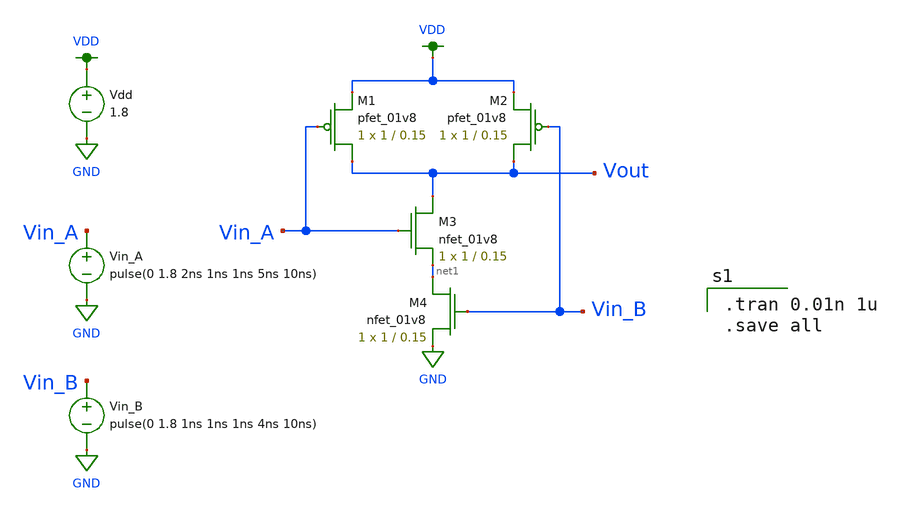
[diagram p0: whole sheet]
** sch_path: MP1/xschem/NAND_tran.sch
**.subckt NAND_tran
Vdd VDD GND 1.8
Vin_A Vin_A GND pulse(0 1.8 2ns 1ns 1ns 5ns 10ns)
XM1 Vout Vin_A VDD VDD sky130_fd_pr__pfet_01v8 L=0.15 W=1 nf=1 ad='int((nf+1)/2) * W/nf * 0.29' as='int((nf+2)/2) * W/nf * 0.29'
+ pd='2*int((nf+1)/2) * (W/nf + 0.29)' ps='2*int((nf+2)/2) * (W/nf + 0.29)' nrd='0.29 / W' nrs='0.29 / W'
+ sa=0 sb=0 sd=0 mult=1 m=1
XM2 Vout Vin_B VDD VDD sky130_fd_pr__pfet_01v8 L=0.15 W=1 nf=1 ad='int((nf+1)/2) * W/nf * 0.29' as='int((nf+2)/2) * W/nf * 0.29'
+ pd='2*int((nf+1)/2) * (W/nf + 0.29)' ps='2*int((nf+2)/2) * (W/nf + 0.29)' nrd='0.29 / W' nrs='0.29 / W'
+ sa=0 sb=0 sd=0 mult=1 m=1
XM3 Vout Vin_A net1 GND sky130_fd_pr__nfet_01v8 L=0.15 W=1 nf=1 ad='int((nf+1)/2) * W/nf * 0.29' as='int((nf+2)/2) * W/nf * 0.29'
+ pd='2*int((nf+1)/2) * (W/nf + 0.29)' ps='2*int((nf+2)/2) * (W/nf + 0.29)' nrd='0.29 / W' nrs='0.29 / W'
+ sa=0 sb=0 sd=0 mult=1 m=1
XM4 net1 Vin_B GND GND sky130_fd_pr__nfet_01v8 L=0.15 W=1 nf=1 ad='int((nf+1)/2) * W/nf * 0.29' as='int((nf+2)/2) * W/nf * 0.29'
+ pd='2*int((nf+1)/2) * (W/nf + 0.29)' ps='2*int((nf+2)/2) * (W/nf + 0.29)' nrd='0.29 / W' nrs='0.29 / W'
+ sa=0 sb=0 sd=0 mult=1 m=1
Vin_B Vin_B GND pulse(0 1.8 1ns 1ns 1ns 4ns 10ns)
**** begin user architecture code

.option wnflag=1
.lib ~/skywater/skywater-pdk/libraries/sky130_fd_pr_ngspice/latest/models/sky130.lib.spice tt


.tran 0.01n 1u
.save all

**** end user architecture code
**.ends
.GLOBAL GND
.GLOBAL VDD
.end
